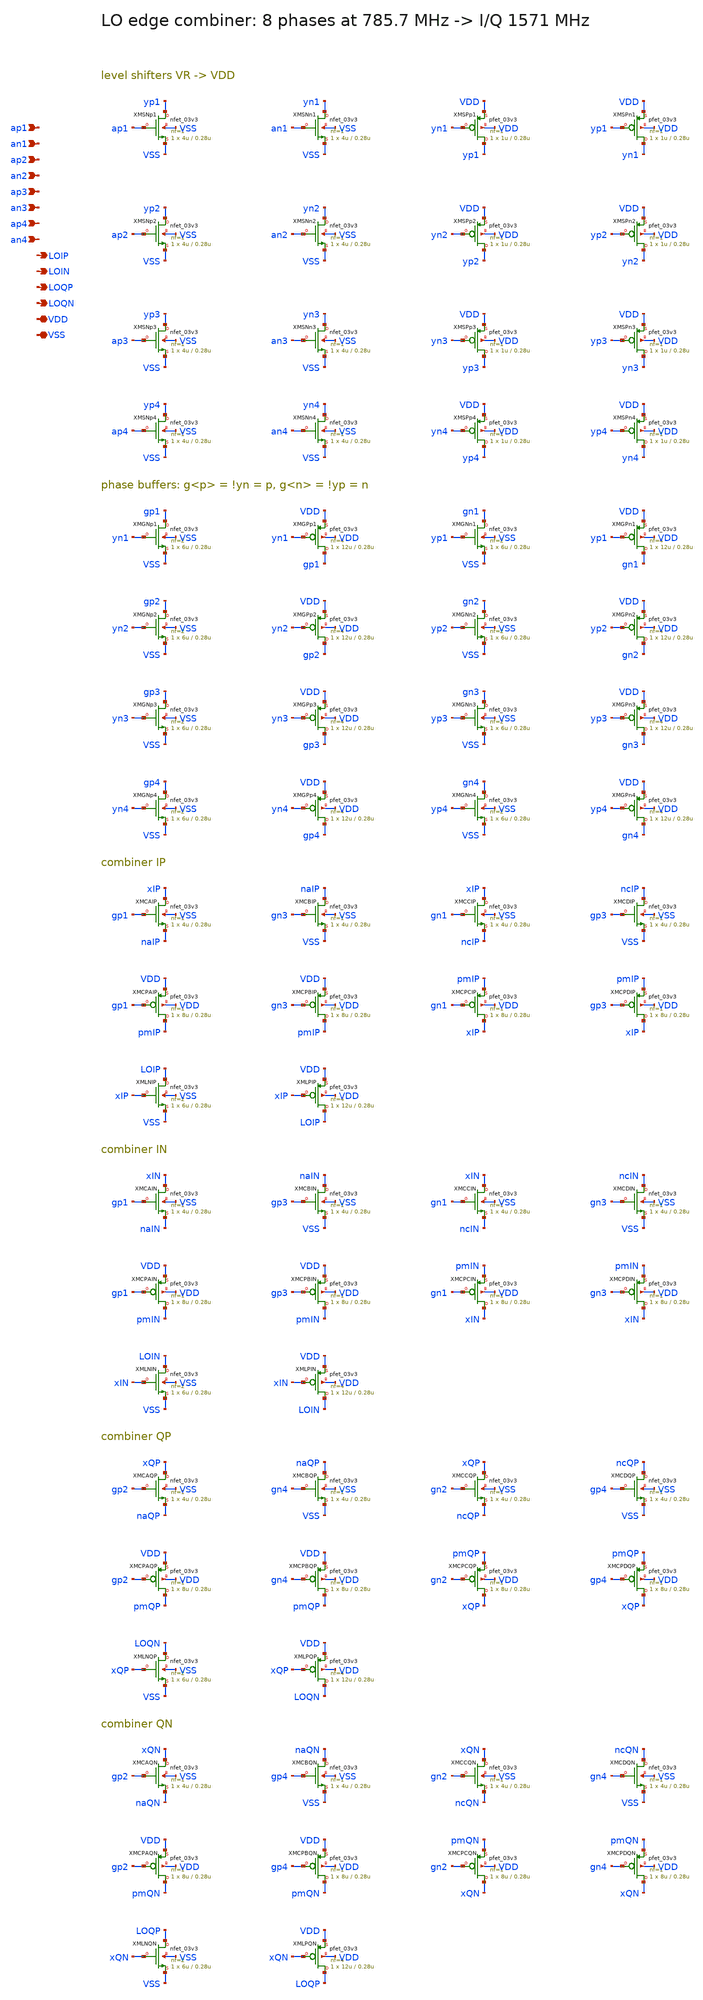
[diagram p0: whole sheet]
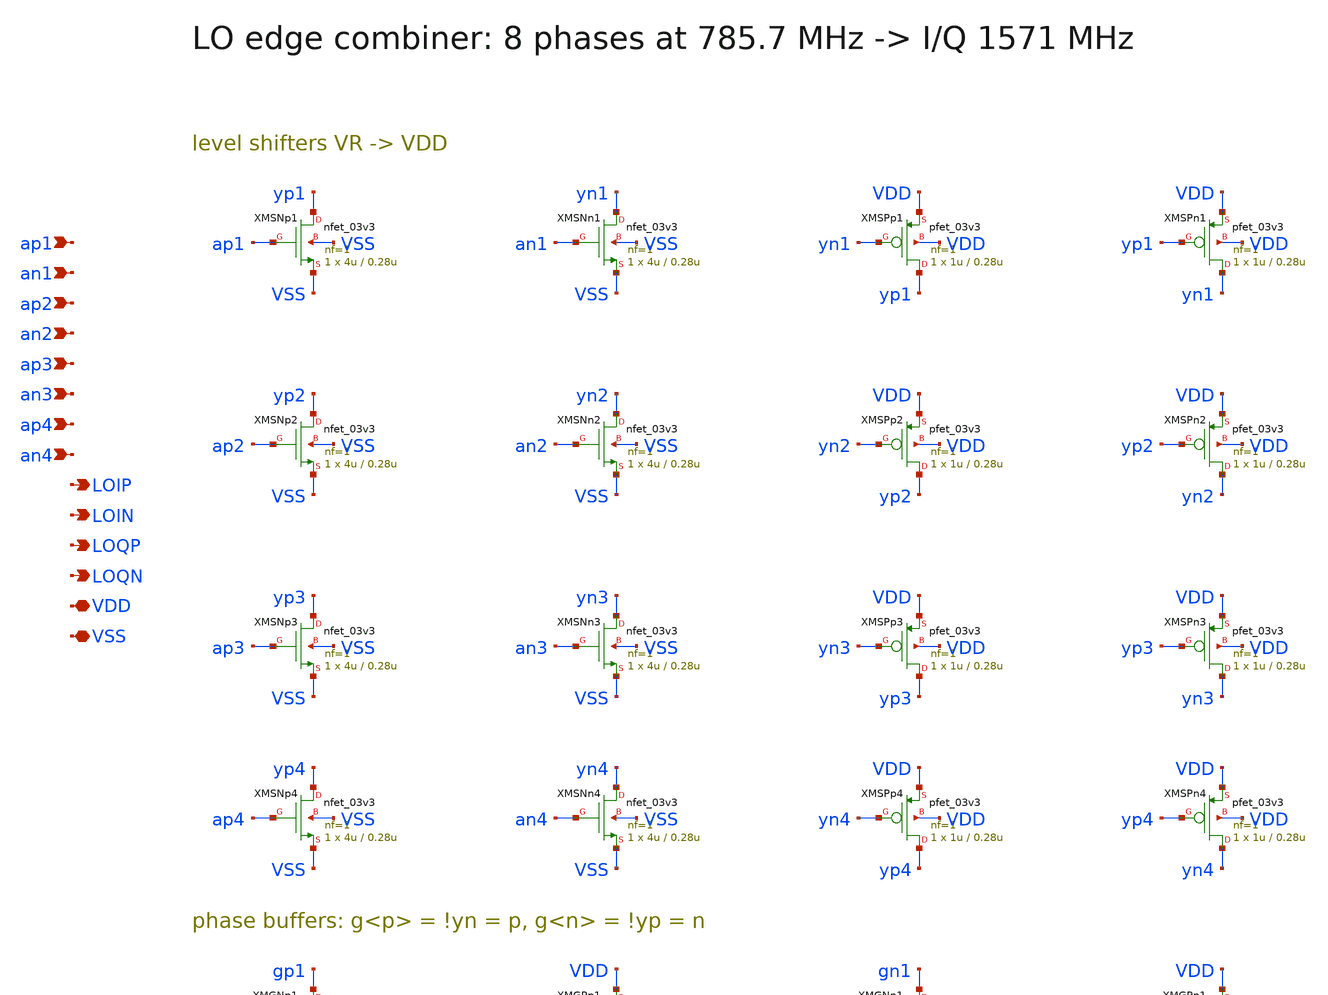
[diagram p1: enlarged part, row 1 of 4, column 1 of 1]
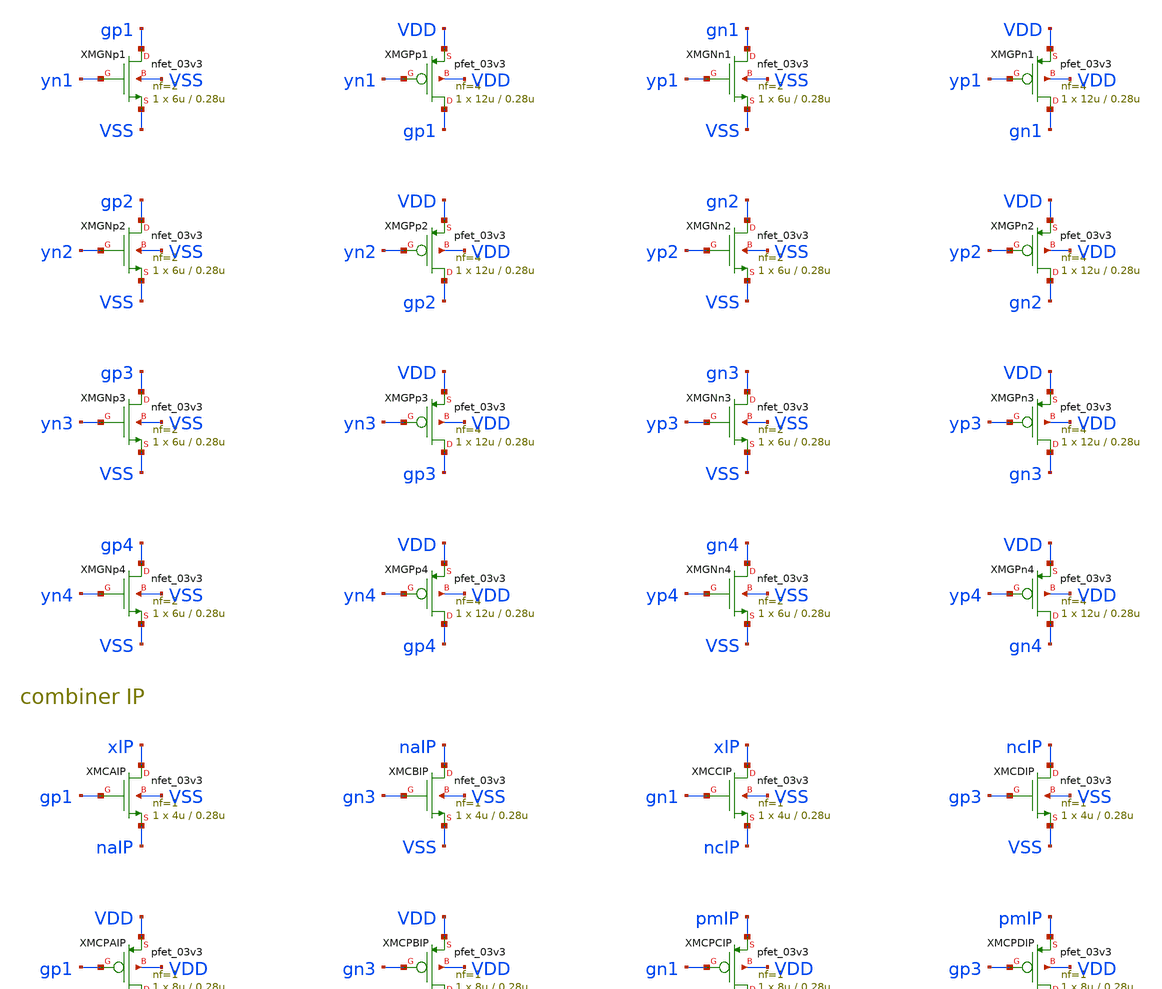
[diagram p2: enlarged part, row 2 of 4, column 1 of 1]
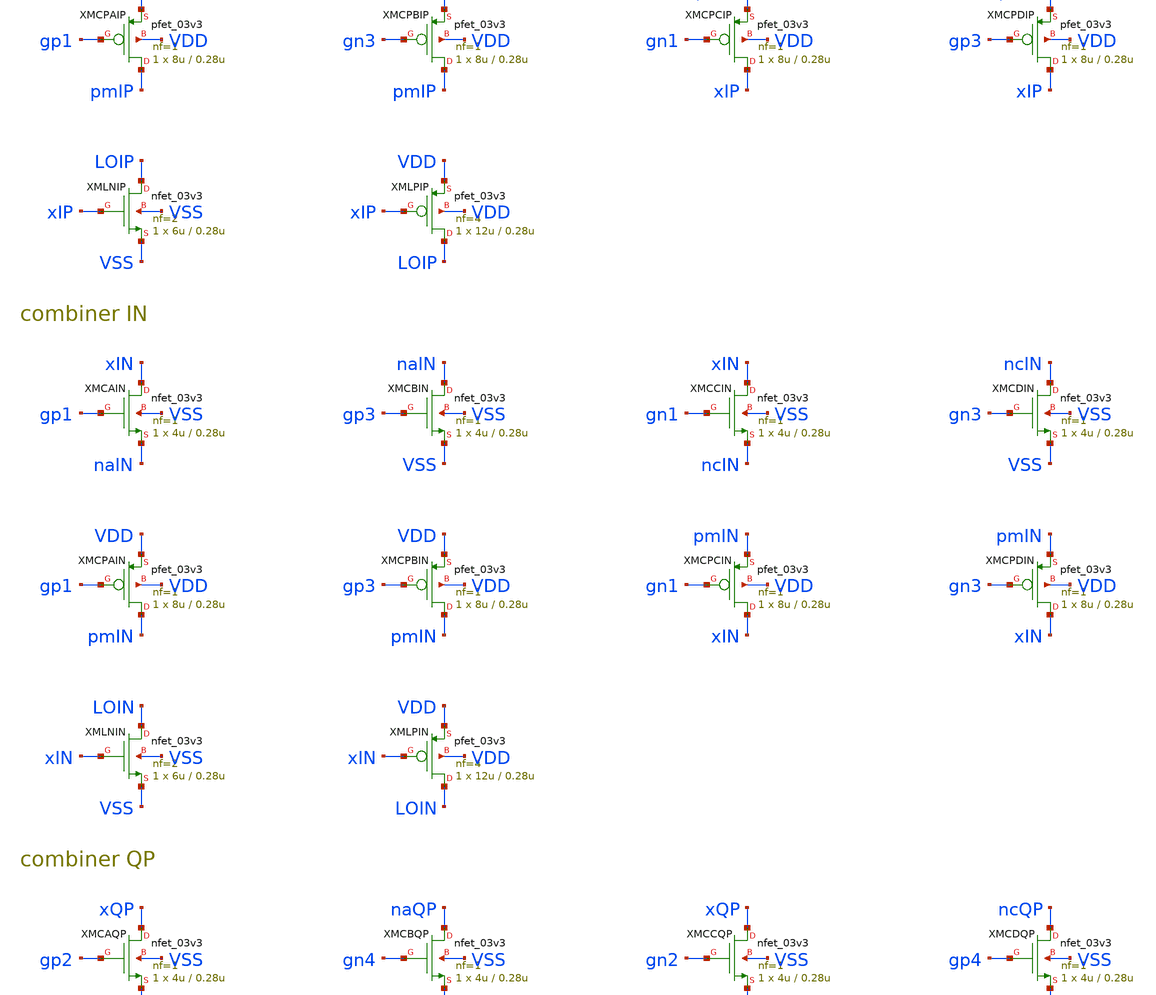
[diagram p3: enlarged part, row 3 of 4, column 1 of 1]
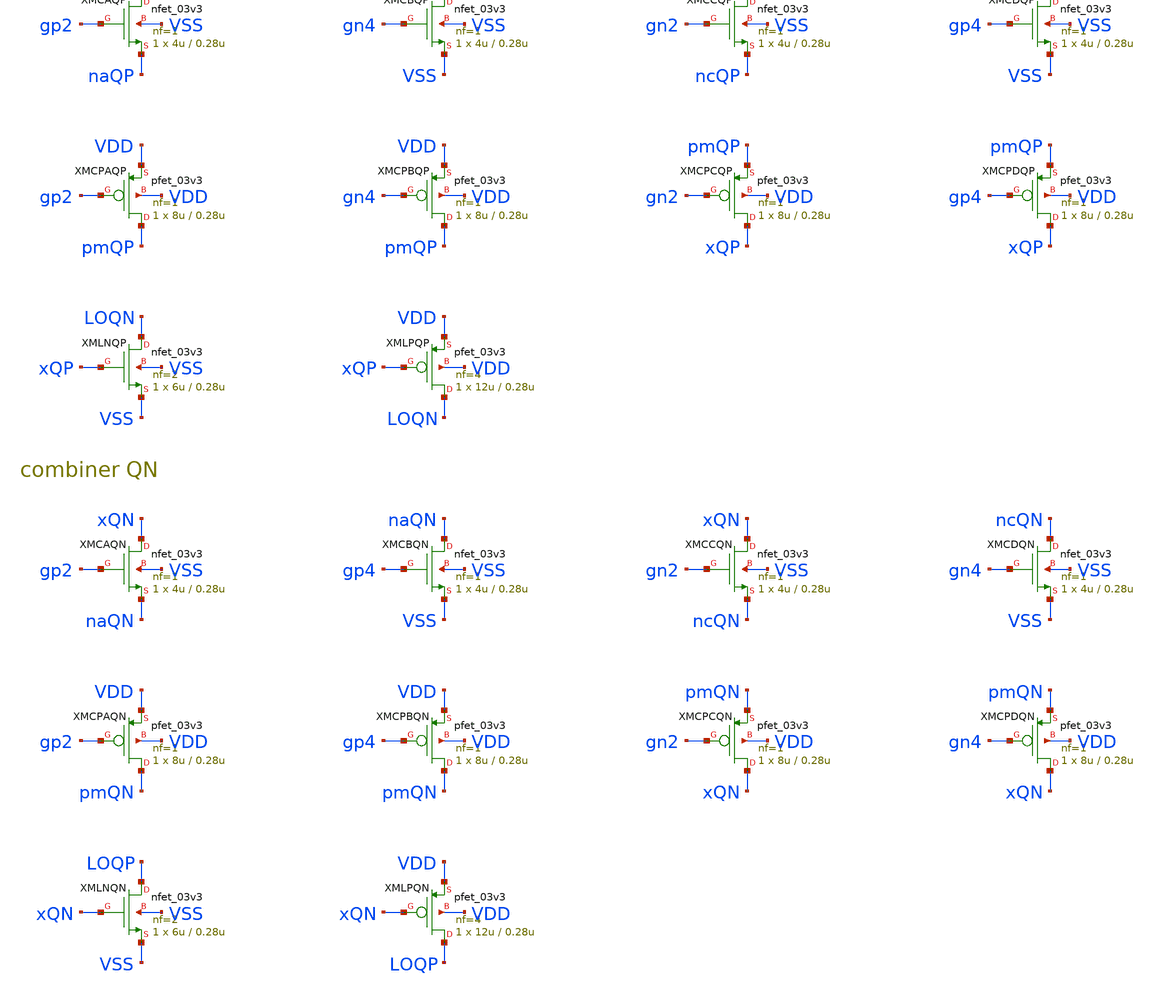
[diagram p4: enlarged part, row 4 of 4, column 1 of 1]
** sch_path: v1_claude/archive/legacy_cells/xschem/lo_comb.sch
**.subckt lo_comb ap1 an1 ap2 an2 ap3 an3 ap4 an4 LOIP LOIN LOQP LOQN VDD VSS
*.ipin ap1
*.ipin an1
*.ipin ap2
*.ipin an2
*.ipin ap3
*.ipin an3
*.ipin ap4
*.ipin an4
*.opin LOIP
*.opin LOIN
*.opin LOQP
*.opin LOQN
*.iopin VDD
*.iopin VSS
XMSNp1 yp1 ap1 VSS VSS nfet_03v3 L=0.28u W=4u nf=1 ad='int((nf+1)/2) * W/nf * 0.18u' as='int((nf+2)/2) * W/nf * 0.18u'
+ pd='2*int((nf+1)/2) * (W/nf + 0.18u)' ps='2*int((nf+2)/2) * (W/nf + 0.18u)' nrd='0.18u / W' nrs='0.18u / W'
+ sa=0 sb=0 sd=0 m=1
XMSNn1 yn1 an1 VSS VSS nfet_03v3 L=0.28u W=4u nf=1 ad='int((nf+1)/2) * W/nf * 0.18u' as='int((nf+2)/2) * W/nf * 0.18u'
+ pd='2*int((nf+1)/2) * (W/nf + 0.18u)' ps='2*int((nf+2)/2) * (W/nf + 0.18u)' nrd='0.18u / W' nrs='0.18u / W'
+ sa=0 sb=0 sd=0 m=1
XMSPp1 yp1 yn1 VDD VDD pfet_03v3 L=0.28u W=1u nf=1 ad='int((nf+1)/2) * W/nf * 0.18u' as='int((nf+2)/2) * W/nf * 0.18u'
+ pd='2*int((nf+1)/2) * (W/nf + 0.18u)' ps='2*int((nf+2)/2) * (W/nf + 0.18u)' nrd='0.18u / W' nrs='0.18u / W'
+ sa=0 sb=0 sd=0 m=1
XMSPn1 yn1 yp1 VDD VDD pfet_03v3 L=0.28u W=1u nf=1 ad='int((nf+1)/2) * W/nf * 0.18u' as='int((nf+2)/2) * W/nf * 0.18u'
+ pd='2*int((nf+1)/2) * (W/nf + 0.18u)' ps='2*int((nf+2)/2) * (W/nf + 0.18u)' nrd='0.18u / W' nrs='0.18u / W'
+ sa=0 sb=0 sd=0 m=1
XMSNp2 yp2 ap2 VSS VSS nfet_03v3 L=0.28u W=4u nf=1 ad='int((nf+1)/2) * W/nf * 0.18u' as='int((nf+2)/2) * W/nf * 0.18u'
+ pd='2*int((nf+1)/2) * (W/nf + 0.18u)' ps='2*int((nf+2)/2) * (W/nf + 0.18u)' nrd='0.18u / W' nrs='0.18u / W'
+ sa=0 sb=0 sd=0 m=1
XMSNn2 yn2 an2 VSS VSS nfet_03v3 L=0.28u W=4u nf=1 ad='int((nf+1)/2) * W/nf * 0.18u' as='int((nf+2)/2) * W/nf * 0.18u'
+ pd='2*int((nf+1)/2) * (W/nf + 0.18u)' ps='2*int((nf+2)/2) * (W/nf + 0.18u)' nrd='0.18u / W' nrs='0.18u / W'
+ sa=0 sb=0 sd=0 m=1
XMSPp2 yp2 yn2 VDD VDD pfet_03v3 L=0.28u W=1u nf=1 ad='int((nf+1)/2) * W/nf * 0.18u' as='int((nf+2)/2) * W/nf * 0.18u'
+ pd='2*int((nf+1)/2) * (W/nf + 0.18u)' ps='2*int((nf+2)/2) * (W/nf + 0.18u)' nrd='0.18u / W' nrs='0.18u / W'
+ sa=0 sb=0 sd=0 m=1
XMSPn2 yn2 yp2 VDD VDD pfet_03v3 L=0.28u W=1u nf=1 ad='int((nf+1)/2) * W/nf * 0.18u' as='int((nf+2)/2) * W/nf * 0.18u'
+ pd='2*int((nf+1)/2) * (W/nf + 0.18u)' ps='2*int((nf+2)/2) * (W/nf + 0.18u)' nrd='0.18u / W' nrs='0.18u / W'
+ sa=0 sb=0 sd=0 m=1
XMSNp3 yp3 ap3 VSS VSS nfet_03v3 L=0.28u W=4u nf=1 ad='int((nf+1)/2) * W/nf * 0.18u' as='int((nf+2)/2) * W/nf * 0.18u'
+ pd='2*int((nf+1)/2) * (W/nf + 0.18u)' ps='2*int((nf+2)/2) * (W/nf + 0.18u)' nrd='0.18u / W' nrs='0.18u / W'
+ sa=0 sb=0 sd=0 m=1
XMSNn3 yn3 an3 VSS VSS nfet_03v3 L=0.28u W=4u nf=1 ad='int((nf+1)/2) * W/nf * 0.18u' as='int((nf+2)/2) * W/nf * 0.18u'
+ pd='2*int((nf+1)/2) * (W/nf + 0.18u)' ps='2*int((nf+2)/2) * (W/nf + 0.18u)' nrd='0.18u / W' nrs='0.18u / W'
+ sa=0 sb=0 sd=0 m=1
XMSPp3 yp3 yn3 VDD VDD pfet_03v3 L=0.28u W=1u nf=1 ad='int((nf+1)/2) * W/nf * 0.18u' as='int((nf+2)/2) * W/nf * 0.18u'
+ pd='2*int((nf+1)/2) * (W/nf + 0.18u)' ps='2*int((nf+2)/2) * (W/nf + 0.18u)' nrd='0.18u / W' nrs='0.18u / W'
+ sa=0 sb=0 sd=0 m=1
XMSPn3 yn3 yp3 VDD VDD pfet_03v3 L=0.28u W=1u nf=1 ad='int((nf+1)/2) * W/nf * 0.18u' as='int((nf+2)/2) * W/nf * 0.18u'
+ pd='2*int((nf+1)/2) * (W/nf + 0.18u)' ps='2*int((nf+2)/2) * (W/nf + 0.18u)' nrd='0.18u / W' nrs='0.18u / W'
+ sa=0 sb=0 sd=0 m=1
XMSNp4 yp4 ap4 VSS VSS nfet_03v3 L=0.28u W=4u nf=1 ad='int((nf+1)/2) * W/nf * 0.18u' as='int((nf+2)/2) * W/nf * 0.18u'
+ pd='2*int((nf+1)/2) * (W/nf + 0.18u)' ps='2*int((nf+2)/2) * (W/nf + 0.18u)' nrd='0.18u / W' nrs='0.18u / W'
+ sa=0 sb=0 sd=0 m=1
XMSNn4 yn4 an4 VSS VSS nfet_03v3 L=0.28u W=4u nf=1 ad='int((nf+1)/2) * W/nf * 0.18u' as='int((nf+2)/2) * W/nf * 0.18u'
+ pd='2*int((nf+1)/2) * (W/nf + 0.18u)' ps='2*int((nf+2)/2) * (W/nf + 0.18u)' nrd='0.18u / W' nrs='0.18u / W'
+ sa=0 sb=0 sd=0 m=1
XMSPp4 yp4 yn4 VDD VDD pfet_03v3 L=0.28u W=1u nf=1 ad='int((nf+1)/2) * W/nf * 0.18u' as='int((nf+2)/2) * W/nf * 0.18u'
+ pd='2*int((nf+1)/2) * (W/nf + 0.18u)' ps='2*int((nf+2)/2) * (W/nf + 0.18u)' nrd='0.18u / W' nrs='0.18u / W'
+ sa=0 sb=0 sd=0 m=1
XMSPn4 yn4 yp4 VDD VDD pfet_03v3 L=0.28u W=1u nf=1 ad='int((nf+1)/2) * W/nf * 0.18u' as='int((nf+2)/2) * W/nf * 0.18u'
+ pd='2*int((nf+1)/2) * (W/nf + 0.18u)' ps='2*int((nf+2)/2) * (W/nf + 0.18u)' nrd='0.18u / W' nrs='0.18u / W'
+ sa=0 sb=0 sd=0 m=1
XMGNp1 gp1 yn1 VSS VSS nfet_03v3 L=0.28u W=6u nf=2 ad='int((nf+1)/2) * W/nf * 0.18u' as='int((nf+2)/2) * W/nf * 0.18u'
+ pd='2*int((nf+1)/2) * (W/nf + 0.18u)' ps='2*int((nf+2)/2) * (W/nf + 0.18u)' nrd='0.18u / W' nrs='0.18u / W'
+ sa=0 sb=0 sd=0 m=1
XMGPp1 gp1 yn1 VDD VDD pfet_03v3 L=0.28u W=12u nf=4 ad='int((nf+1)/2) * W/nf * 0.18u' as='int((nf+2)/2) * W/nf * 0.18u'
+ pd='2*int((nf+1)/2) * (W/nf + 0.18u)' ps='2*int((nf+2)/2) * (W/nf + 0.18u)' nrd='0.18u / W' nrs='0.18u / W'
+ sa=0 sb=0 sd=0 m=1
XMGNn1 gn1 yp1 VSS VSS nfet_03v3 L=0.28u W=6u nf=2 ad='int((nf+1)/2) * W/nf * 0.18u' as='int((nf+2)/2) * W/nf * 0.18u'
+ pd='2*int((nf+1)/2) * (W/nf + 0.18u)' ps='2*int((nf+2)/2) * (W/nf + 0.18u)' nrd='0.18u / W' nrs='0.18u / W'
+ sa=0 sb=0 sd=0 m=1
XMGPn1 gn1 yp1 VDD VDD pfet_03v3 L=0.28u W=12u nf=4 ad='int((nf+1)/2) * W/nf * 0.18u' as='int((nf+2)/2) * W/nf * 0.18u'
+ pd='2*int((nf+1)/2) * (W/nf + 0.18u)' ps='2*int((nf+2)/2) * (W/nf + 0.18u)' nrd='0.18u / W' nrs='0.18u / W'
+ sa=0 sb=0 sd=0 m=1
XMGNp2 gp2 yn2 VSS VSS nfet_03v3 L=0.28u W=6u nf=2 ad='int((nf+1)/2) * W/nf * 0.18u' as='int((nf+2)/2) * W/nf * 0.18u'
+ pd='2*int((nf+1)/2) * (W/nf + 0.18u)' ps='2*int((nf+2)/2) * (W/nf + 0.18u)' nrd='0.18u / W' nrs='0.18u / W'
+ sa=0 sb=0 sd=0 m=1
XMGPp2 gp2 yn2 VDD VDD pfet_03v3 L=0.28u W=12u nf=4 ad='int((nf+1)/2) * W/nf * 0.18u' as='int((nf+2)/2) * W/nf * 0.18u'
+ pd='2*int((nf+1)/2) * (W/nf + 0.18u)' ps='2*int((nf+2)/2) * (W/nf + 0.18u)' nrd='0.18u / W' nrs='0.18u / W'
+ sa=0 sb=0 sd=0 m=1
XMGNn2 gn2 yp2 VSS VSS nfet_03v3 L=0.28u W=6u nf=2 ad='int((nf+1)/2) * W/nf * 0.18u' as='int((nf+2)/2) * W/nf * 0.18u'
+ pd='2*int((nf+1)/2) * (W/nf + 0.18u)' ps='2*int((nf+2)/2) * (W/nf + 0.18u)' nrd='0.18u / W' nrs='0.18u / W'
+ sa=0 sb=0 sd=0 m=1
XMGPn2 gn2 yp2 VDD VDD pfet_03v3 L=0.28u W=12u nf=4 ad='int((nf+1)/2) * W/nf * 0.18u' as='int((nf+2)/2) * W/nf * 0.18u'
+ pd='2*int((nf+1)/2) * (W/nf + 0.18u)' ps='2*int((nf+2)/2) * (W/nf + 0.18u)' nrd='0.18u / W' nrs='0.18u / W'
+ sa=0 sb=0 sd=0 m=1
XMGNp3 gp3 yn3 VSS VSS nfet_03v3 L=0.28u W=6u nf=2 ad='int((nf+1)/2) * W/nf * 0.18u' as='int((nf+2)/2) * W/nf * 0.18u'
+ pd='2*int((nf+1)/2) * (W/nf + 0.18u)' ps='2*int((nf+2)/2) * (W/nf + 0.18u)' nrd='0.18u / W' nrs='0.18u / W'
+ sa=0 sb=0 sd=0 m=1
XMGPp3 gp3 yn3 VDD VDD pfet_03v3 L=0.28u W=12u nf=4 ad='int((nf+1)/2) * W/nf * 0.18u' as='int((nf+2)/2) * W/nf * 0.18u'
+ pd='2*int((nf+1)/2) * (W/nf + 0.18u)' ps='2*int((nf+2)/2) * (W/nf + 0.18u)' nrd='0.18u / W' nrs='0.18u / W'
+ sa=0 sb=0 sd=0 m=1
XMGNn3 gn3 yp3 VSS VSS nfet_03v3 L=0.28u W=6u nf=2 ad='int((nf+1)/2) * W/nf * 0.18u' as='int((nf+2)/2) * W/nf * 0.18u'
+ pd='2*int((nf+1)/2) * (W/nf + 0.18u)' ps='2*int((nf+2)/2) * (W/nf + 0.18u)' nrd='0.18u / W' nrs='0.18u / W'
+ sa=0 sb=0 sd=0 m=1
XMGPn3 gn3 yp3 VDD VDD pfet_03v3 L=0.28u W=12u nf=4 ad='int((nf+1)/2) * W/nf * 0.18u' as='int((nf+2)/2) * W/nf * 0.18u'
+ pd='2*int((nf+1)/2) * (W/nf + 0.18u)' ps='2*int((nf+2)/2) * (W/nf + 0.18u)' nrd='0.18u / W' nrs='0.18u / W'
+ sa=0 sb=0 sd=0 m=1
XMGNp4 gp4 yn4 VSS VSS nfet_03v3 L=0.28u W=6u nf=2 ad='int((nf+1)/2) * W/nf * 0.18u' as='int((nf+2)/2) * W/nf * 0.18u'
+ pd='2*int((nf+1)/2) * (W/nf + 0.18u)' ps='2*int((nf+2)/2) * (W/nf + 0.18u)' nrd='0.18u / W' nrs='0.18u / W'
+ sa=0 sb=0 sd=0 m=1
XMGPp4 gp4 yn4 VDD VDD pfet_03v3 L=0.28u W=12u nf=4 ad='int((nf+1)/2) * W/nf * 0.18u' as='int((nf+2)/2) * W/nf * 0.18u'
+ pd='2*int((nf+1)/2) * (W/nf + 0.18u)' ps='2*int((nf+2)/2) * (W/nf + 0.18u)' nrd='0.18u / W' nrs='0.18u / W'
+ sa=0 sb=0 sd=0 m=1
XMGNn4 gn4 yp4 VSS VSS nfet_03v3 L=0.28u W=6u nf=2 ad='int((nf+1)/2) * W/nf * 0.18u' as='int((nf+2)/2) * W/nf * 0.18u'
+ pd='2*int((nf+1)/2) * (W/nf + 0.18u)' ps='2*int((nf+2)/2) * (W/nf + 0.18u)' nrd='0.18u / W' nrs='0.18u / W'
+ sa=0 sb=0 sd=0 m=1
XMGPn4 gn4 yp4 VDD VDD pfet_03v3 L=0.28u W=12u nf=4 ad='int((nf+1)/2) * W/nf * 0.18u' as='int((nf+2)/2) * W/nf * 0.18u'
+ pd='2*int((nf+1)/2) * (W/nf + 0.18u)' ps='2*int((nf+2)/2) * (W/nf + 0.18u)' nrd='0.18u / W' nrs='0.18u / W'
+ sa=0 sb=0 sd=0 m=1
XMCAIP xIP gp1 naIP VSS nfet_03v3 L=0.28u W=4u nf=1 ad='int((nf+1)/2) * W/nf * 0.18u' as='int((nf+2)/2) * W/nf * 0.18u'
+ pd='2*int((nf+1)/2) * (W/nf + 0.18u)' ps='2*int((nf+2)/2) * (W/nf + 0.18u)' nrd='0.18u / W' nrs='0.18u / W'
+ sa=0 sb=0 sd=0 m=1
XMCBIP naIP gn3 VSS VSS nfet_03v3 L=0.28u W=4u nf=1 ad='int((nf+1)/2) * W/nf * 0.18u' as='int((nf+2)/2) * W/nf * 0.18u'
+ pd='2*int((nf+1)/2) * (W/nf + 0.18u)' ps='2*int((nf+2)/2) * (W/nf + 0.18u)' nrd='0.18u / W' nrs='0.18u / W'
+ sa=0 sb=0 sd=0 m=1
XMCCIP xIP gn1 ncIP VSS nfet_03v3 L=0.28u W=4u nf=1 ad='int((nf+1)/2) * W/nf * 0.18u' as='int((nf+2)/2) * W/nf * 0.18u'
+ pd='2*int((nf+1)/2) * (W/nf + 0.18u)' ps='2*int((nf+2)/2) * (W/nf + 0.18u)' nrd='0.18u / W' nrs='0.18u / W'
+ sa=0 sb=0 sd=0 m=1
XMCDIP ncIP gp3 VSS VSS nfet_03v3 L=0.28u W=4u nf=1 ad='int((nf+1)/2) * W/nf * 0.18u' as='int((nf+2)/2) * W/nf * 0.18u'
+ pd='2*int((nf+1)/2) * (W/nf + 0.18u)' ps='2*int((nf+2)/2) * (W/nf + 0.18u)' nrd='0.18u / W' nrs='0.18u / W'
+ sa=0 sb=0 sd=0 m=1
XMCPAIP pmIP gp1 VDD VDD pfet_03v3 L=0.28u W=8u nf=1 ad='int((nf+1)/2) * W/nf * 0.18u' as='int((nf+2)/2) * W/nf * 0.18u'
+ pd='2*int((nf+1)/2) * (W/nf + 0.18u)' ps='2*int((nf+2)/2) * (W/nf + 0.18u)' nrd='0.18u / W' nrs='0.18u / W'
+ sa=0 sb=0 sd=0 m=1
XMCPBIP pmIP gn3 VDD VDD pfet_03v3 L=0.28u W=8u nf=1 ad='int((nf+1)/2) * W/nf * 0.18u' as='int((nf+2)/2) * W/nf * 0.18u'
+ pd='2*int((nf+1)/2) * (W/nf + 0.18u)' ps='2*int((nf+2)/2) * (W/nf + 0.18u)' nrd='0.18u / W' nrs='0.18u / W'
+ sa=0 sb=0 sd=0 m=1
XMCPCIP xIP gn1 pmIP VDD pfet_03v3 L=0.28u W=8u nf=1 ad='int((nf+1)/2) * W/nf * 0.18u' as='int((nf+2)/2) * W/nf * 0.18u'
+ pd='2*int((nf+1)/2) * (W/nf + 0.18u)' ps='2*int((nf+2)/2) * (W/nf + 0.18u)' nrd='0.18u / W' nrs='0.18u / W'
+ sa=0 sb=0 sd=0 m=1
XMCPDIP xIP gp3 pmIP VDD pfet_03v3 L=0.28u W=8u nf=1 ad='int((nf+1)/2) * W/nf * 0.18u' as='int((nf+2)/2) * W/nf * 0.18u'
+ pd='2*int((nf+1)/2) * (W/nf + 0.18u)' ps='2*int((nf+2)/2) * (W/nf + 0.18u)' nrd='0.18u / W' nrs='0.18u / W'
+ sa=0 sb=0 sd=0 m=1
XMLNIP LOIP xIP VSS VSS nfet_03v3 L=0.28u W=6u nf=2 ad='int((nf+1)/2) * W/nf * 0.18u' as='int((nf+2)/2) * W/nf * 0.18u'
+ pd='2*int((nf+1)/2) * (W/nf + 0.18u)' ps='2*int((nf+2)/2) * (W/nf + 0.18u)' nrd='0.18u / W' nrs='0.18u / W'
+ sa=0 sb=0 sd=0 m=1
XMLPIP LOIP xIP VDD VDD pfet_03v3 L=0.28u W=12u nf=4 ad='int((nf+1)/2) * W/nf * 0.18u' as='int((nf+2)/2) * W/nf * 0.18u'
+ pd='2*int((nf+1)/2) * (W/nf + 0.18u)' ps='2*int((nf+2)/2) * (W/nf + 0.18u)' nrd='0.18u / W' nrs='0.18u / W'
+ sa=0 sb=0 sd=0 m=1
XMCAIN xIN gp1 naIN VSS nfet_03v3 L=0.28u W=4u nf=1 ad='int((nf+1)/2) * W/nf * 0.18u' as='int((nf+2)/2) * W/nf * 0.18u'
+ pd='2*int((nf+1)/2) * (W/nf + 0.18u)' ps='2*int((nf+2)/2) * (W/nf + 0.18u)' nrd='0.18u / W' nrs='0.18u / W'
+ sa=0 sb=0 sd=0 m=1
XMCBIN naIN gp3 VSS VSS nfet_03v3 L=0.28u W=4u nf=1 ad='int((nf+1)/2) * W/nf * 0.18u' as='int((nf+2)/2) * W/nf * 0.18u'
+ pd='2*int((nf+1)/2) * (W/nf + 0.18u)' ps='2*int((nf+2)/2) * (W/nf + 0.18u)' nrd='0.18u / W' nrs='0.18u / W'
+ sa=0 sb=0 sd=0 m=1
XMCCIN xIN gn1 ncIN VSS nfet_03v3 L=0.28u W=4u nf=1 ad='int((nf+1)/2) * W/nf * 0.18u' as='int((nf+2)/2) * W/nf * 0.18u'
+ pd='2*int((nf+1)/2) * (W/nf + 0.18u)' ps='2*int((nf+2)/2) * (W/nf + 0.18u)' nrd='0.18u / W' nrs='0.18u / W'
+ sa=0 sb=0 sd=0 m=1
XMCDIN ncIN gn3 VSS VSS nfet_03v3 L=0.28u W=4u nf=1 ad='int((nf+1)/2) * W/nf * 0.18u' as='int((nf+2)/2) * W/nf * 0.18u'
+ pd='2*int((nf+1)/2) * (W/nf + 0.18u)' ps='2*int((nf+2)/2) * (W/nf + 0.18u)' nrd='0.18u / W' nrs='0.18u / W'
+ sa=0 sb=0 sd=0 m=1
XMCPAIN pmIN gp1 VDD VDD pfet_03v3 L=0.28u W=8u nf=1 ad='int((nf+1)/2) * W/nf * 0.18u' as='int((nf+2)/2) * W/nf * 0.18u'
+ pd='2*int((nf+1)/2) * (W/nf + 0.18u)' ps='2*int((nf+2)/2) * (W/nf + 0.18u)' nrd='0.18u / W' nrs='0.18u / W'
+ sa=0 sb=0 sd=0 m=1
XMCPBIN pmIN gp3 VDD VDD pfet_03v3 L=0.28u W=8u nf=1 ad='int((nf+1)/2) * W/nf * 0.18u' as='int((nf+2)/2) * W/nf * 0.18u'
+ pd='2*int((nf+1)/2) * (W/nf + 0.18u)' ps='2*int((nf+2)/2) * (W/nf + 0.18u)' nrd='0.18u / W' nrs='0.18u / W'
+ sa=0 sb=0 sd=0 m=1
XMCPCIN xIN gn1 pmIN VDD pfet_03v3 L=0.28u W=8u nf=1 ad='int((nf+1)/2) * W/nf * 0.18u' as='int((nf+2)/2) * W/nf * 0.18u'
+ pd='2*int((nf+1)/2) * (W/nf + 0.18u)' ps='2*int((nf+2)/2) * (W/nf + 0.18u)' nrd='0.18u / W' nrs='0.18u / W'
+ sa=0 sb=0 sd=0 m=1
XMCPDIN xIN gn3 pmIN VDD pfet_03v3 L=0.28u W=8u nf=1 ad='int((nf+1)/2) * W/nf * 0.18u' as='int((nf+2)/2) * W/nf * 0.18u'
+ pd='2*int((nf+1)/2) * (W/nf + 0.18u)' ps='2*int((nf+2)/2) * (W/nf + 0.18u)' nrd='0.18u / W' nrs='0.18u / W'
+ sa=0 sb=0 sd=0 m=1
XMLNIN LOIN xIN VSS VSS nfet_03v3 L=0.28u W=6u nf=2 ad='int((nf+1)/2) * W/nf * 0.18u' as='int((nf+2)/2) * W/nf * 0.18u'
+ pd='2*int((nf+1)/2) * (W/nf + 0.18u)' ps='2*int((nf+2)/2) * (W/nf + 0.18u)' nrd='0.18u / W' nrs='0.18u / W'
+ sa=0 sb=0 sd=0 m=1
XMLPIN LOIN xIN VDD VDD pfet_03v3 L=0.28u W=12u nf=4 ad='int((nf+1)/2) * W/nf * 0.18u' as='int((nf+2)/2) * W/nf * 0.18u'
+ pd='2*int((nf+1)/2) * (W/nf + 0.18u)' ps='2*int((nf+2)/2) * (W/nf + 0.18u)' nrd='0.18u / W' nrs='0.18u / W'
+ sa=0 sb=0 sd=0 m=1
XMCAQP xQP gp2 naQP VSS nfet_03v3 L=0.28u W=4u nf=1 ad='int((nf+1)/2) * W/nf * 0.18u' as='int((nf+2)/2) * W/nf * 0.18u'
+ pd='2*int((nf+1)/2) * (W/nf + 0.18u)' ps='2*int((nf+2)/2) * (W/nf + 0.18u)' nrd='0.18u / W' nrs='0.18u / W'
+ sa=0 sb=0 sd=0 m=1
XMCBQP naQP gn4 VSS VSS nfet_03v3 L=0.28u W=4u nf=1 ad='int((nf+1)/2) * W/nf * 0.18u' as='int((nf+2)/2) * W/nf * 0.18u'
+ pd='2*int((nf+1)/2) * (W/nf + 0.18u)' ps='2*int((nf+2)/2) * (W/nf + 0.18u)' nrd='0.18u / W' nrs='0.18u / W'
+ sa=0 sb=0 sd=0 m=1
XMCCQP xQP gn2 ncQP VSS nfet_03v3 L=0.28u W=4u nf=1 ad='int((nf+1)/2) * W/nf * 0.18u' as='int((nf+2)/2) * W/nf * 0.18u'
+ pd='2*int((nf+1)/2) * (W/nf + 0.18u)' ps='2*int((nf+2)/2) * (W/nf + 0.18u)' nrd='0.18u / W' nrs='0.18u / W'
+ sa=0 sb=0 sd=0 m=1
XMCDQP ncQP gp4 VSS VSS nfet_03v3 L=0.28u W=4u nf=1 ad='int((nf+1)/2) * W/nf * 0.18u' as='int((nf+2)/2) * W/nf * 0.18u'
+ pd='2*int((nf+1)/2) * (W/nf + 0.18u)' ps='2*int((nf+2)/2) * (W/nf + 0.18u)' nrd='0.18u / W' nrs='0.18u / W'
+ sa=0 sb=0 sd=0 m=1
XMCPAQP pmQP gp2 VDD VDD pfet_03v3 L=0.28u W=8u nf=1 ad='int((nf+1)/2) * W/nf * 0.18u' as='int((nf+2)/2) * W/nf * 0.18u'
+ pd='2*int((nf+1)/2) * (W/nf + 0.18u)' ps='2*int((nf+2)/2) * (W/nf + 0.18u)' nrd='0.18u / W' nrs='0.18u / W'
+ sa=0 sb=0 sd=0 m=1
XMCPBQP pmQP gn4 VDD VDD pfet_03v3 L=0.28u W=8u nf=1 ad='int((nf+1)/2) * W/nf * 0.18u' as='int((nf+2)/2) * W/nf * 0.18u'
+ pd='2*int((nf+1)/2) * (W/nf + 0.18u)' ps='2*int((nf+2)/2) * (W/nf + 0.18u)' nrd='0.18u / W' nrs='0.18u / W'
+ sa=0 sb=0 sd=0 m=1
XMCPCQP xQP gn2 pmQP VDD pfet_03v3 L=0.28u W=8u nf=1 ad='int((nf+1)/2) * W/nf * 0.18u' as='int((nf+2)/2) * W/nf * 0.18u'
+ pd='2*int((nf+1)/2) * (W/nf + 0.18u)' ps='2*int((nf+2)/2) * (W/nf + 0.18u)' nrd='0.18u / W' nrs='0.18u / W'
+ sa=0 sb=0 sd=0 m=1
XMCPDQP xQP gp4 pmQP VDD pfet_03v3 L=0.28u W=8u nf=1 ad='int((nf+1)/2) * W/nf * 0.18u' as='int((nf+2)/2) * W/nf * 0.18u'
+ pd='2*int((nf+1)/2) * (W/nf + 0.18u)' ps='2*int((nf+2)/2) * (W/nf + 0.18u)' nrd='0.18u / W' nrs='0.18u / W'
+ sa=0 sb=0 sd=0 m=1
XMLNQP LOQN xQP VSS VSS nfet_03v3 L=0.28u W=6u nf=2 ad='int((nf+1)/2) * W/nf * 0.18u' as='int((nf+2)/2) * W/nf * 0.18u'
+ pd='2*int((nf+1)/2) * (W/nf + 0.18u)' ps='2*int((nf+2)/2) * (W/nf + 0.18u)' nrd='0.18u / W' nrs='0.18u / W'
+ sa=0 sb=0 sd=0 m=1
XMLPQP LOQN xQP VDD VDD pfet_03v3 L=0.28u W=12u nf=4 ad='int((nf+1)/2) * W/nf * 0.18u' as='int((nf+2)/2) * W/nf * 0.18u'
+ pd='2*int((nf+1)/2) * (W/nf + 0.18u)' ps='2*int((nf+2)/2) * (W/nf + 0.18u)' nrd='0.18u / W' nrs='0.18u / W'
+ sa=0 sb=0 sd=0 m=1
XMCAQN xQN gp2 naQN VSS nfet_03v3 L=0.28u W=4u nf=1 ad='int((nf+1)/2) * W/nf * 0.18u' as='int((nf+2)/2) * W/nf * 0.18u'
+ pd='2*int((nf+1)/2) * (W/nf + 0.18u)' ps='2*int((nf+2)/2) * (W/nf + 0.18u)' nrd='0.18u / W' nrs='0.18u / W'
+ sa=0 sb=0 sd=0 m=1
XMCBQN naQN gp4 VSS VSS nfet_03v3 L=0.28u W=4u nf=1 ad='int((nf+1)/2) * W/nf * 0.18u' as='int((nf+2)/2) * W/nf * 0.18u'
+ pd='2*int((nf+1)/2) * (W/nf + 0.18u)' ps='2*int((nf+2)/2) * (W/nf + 0.18u)' nrd='0.18u / W' nrs='0.18u / W'
+ sa=0 sb=0 sd=0 m=1
XMCCQN xQN gn2 ncQN VSS nfet_03v3 L=0.28u W=4u nf=1 ad='int((nf+1)/2) * W/nf * 0.18u' as='int((nf+2)/2) * W/nf * 0.18u'
+ pd='2*int((nf+1)/2) * (W/nf + 0.18u)' ps='2*int((nf+2)/2) * (W/nf + 0.18u)' nrd='0.18u / W' nrs='0.18u / W'
+ sa=0 sb=0 sd=0 m=1
XMCDQN ncQN gn4 VSS VSS nfet_03v3 L=0.28u W=4u nf=1 ad='int((nf+1)/2) * W/nf * 0.18u' as='int((nf+2)/2) * W/nf * 0.18u'
+ pd='2*int((nf+1)/2) * (W/nf + 0.18u)' ps='2*int((nf+2)/2) * (W/nf + 0.18u)' nrd='0.18u / W' nrs='0.18u / W'
+ sa=0 sb=0 sd=0 m=1
XMCPAQN pmQN gp2 VDD VDD pfet_03v3 L=0.28u W=8u nf=1 ad='int((nf+1)/2) * W/nf * 0.18u' as='int((nf+2)/2) * W/nf * 0.18u'
+ pd='2*int((nf+1)/2) * (W/nf + 0.18u)' ps='2*int((nf+2)/2) * (W/nf + 0.18u)' nrd='0.18u / W' nrs='0.18u / W'
+ sa=0 sb=0 sd=0 m=1
XMCPBQN pmQN gp4 VDD VDD pfet_03v3 L=0.28u W=8u nf=1 ad='int((nf+1)/2) * W/nf * 0.18u' as='int((nf+2)/2) * W/nf * 0.18u'
+ pd='2*int((nf+1)/2) * (W/nf + 0.18u)' ps='2*int((nf+2)/2) * (W/nf + 0.18u)' nrd='0.18u / W' nrs='0.18u / W'
+ sa=0 sb=0 sd=0 m=1
XMCPCQN xQN gn2 pmQN VDD pfet_03v3 L=0.28u W=8u nf=1 ad='int((nf+1)/2) * W/nf * 0.18u' as='int((nf+2)/2) * W/nf * 0.18u'
+ pd='2*int((nf+1)/2) * (W/nf + 0.18u)' ps='2*int((nf+2)/2) * (W/nf + 0.18u)' nrd='0.18u / W' nrs='0.18u / W'
+ sa=0 sb=0 sd=0 m=1
XMCPDQN xQN gn4 pmQN VDD pfet_03v3 L=0.28u W=8u nf=1 ad='int((nf+1)/2) * W/nf * 0.18u' as='int((nf+2)/2) * W/nf * 0.18u'
+ pd='2*int((nf+1)/2) * (W/nf + 0.18u)' ps='2*int((nf+2)/2) * (W/nf + 0.18u)' nrd='0.18u / W' nrs='0.18u / W'
+ sa=0 sb=0 sd=0 m=1
XMLNQN LOQP xQN VSS VSS nfet_03v3 L=0.28u W=6u nf=2 ad='int((nf+1)/2) * W/nf * 0.18u' as='int((nf+2)/2) * W/nf * 0.18u'
+ pd='2*int((nf+1)/2) * (W/nf + 0.18u)' ps='2*int((nf+2)/2) * (W/nf + 0.18u)' nrd='0.18u / W' nrs='0.18u / W'
+ sa=0 sb=0 sd=0 m=1
XMLPQN LOQP xQN VDD VDD pfet_03v3 L=0.28u W=12u nf=4 ad='int((nf+1)/2) * W/nf * 0.18u' as='int((nf+2)/2) * W/nf * 0.18u'
+ pd='2*int((nf+1)/2) * (W/nf + 0.18u)' ps='2*int((nf+2)/2) * (W/nf + 0.18u)' nrd='0.18u / W' nrs='0.18u / W'
+ sa=0 sb=0 sd=0 m=1
**.ends
.end
